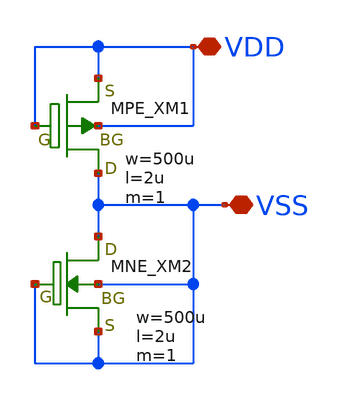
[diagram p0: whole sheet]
** sch_path: libs.tech/xschem/TR-1um_frame/OSS_ESD_5V_VSS.sch
**.subckt OSS_ESD_5V_VSS VSS VDD
*.iopin VSS
*.iopin VDD
XXM1 VSS VDD VDD VDD MPE w=500u l=2u as=0 ad=0 ps=0 pd=0 nrd=0 nrs=0 m=1
XXM2 VSS VSS VSS VSS MNE w=500u l=2u as=0 ad=0 ps=0 pd=0 nrd=0 nrs=0 m=1
**.ends
.end
